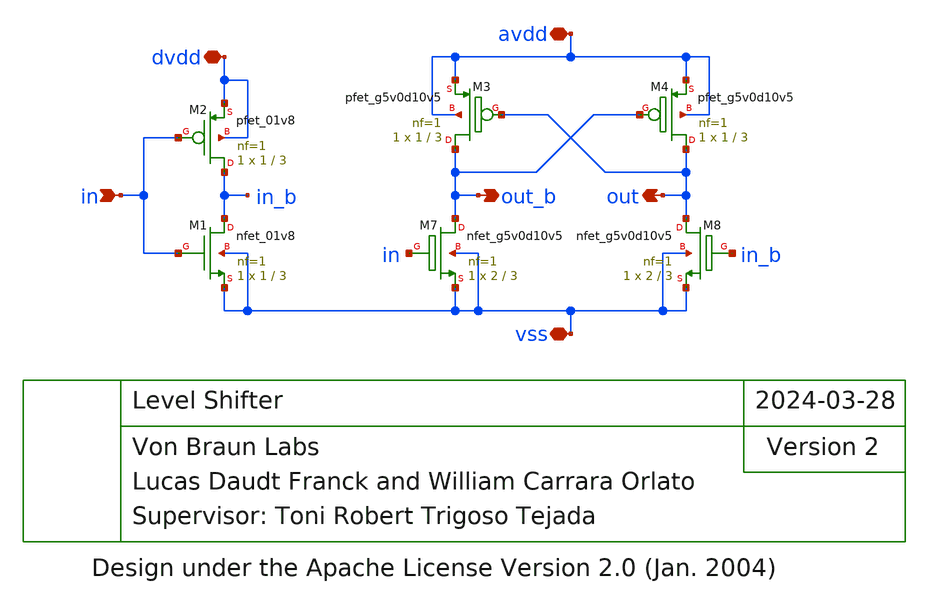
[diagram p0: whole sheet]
** sch_path: xschem/level_shifter.sch
* Design under the Apache License Version 2.0 (Jan. 2004)
**.subckt level_shifter avdd out_b out vss dvdd in
*.iopin avdd
*.opin out_b
*.opin out
*.iopin vss
*.iopin dvdd
*.ipin in
XM1 in_b in vss vss sky130_fd_pr__nfet_01v8 L=3 W=1 nf=1 ad='int((nf+1)/2) * W/nf * 0.29' as='int((nf+2)/2) * W/nf * 0.29'
+ pd='2*int((nf+1)/2) * (W/nf + 0.29)' ps='2*int((nf+2)/2) * (W/nf + 0.29)' nrd='0.29 / W' nrs='0.29 / W'
+ sa=0 sb=0 sd=0 mult=1 m=1
XM2 in_b in dvdd dvdd sky130_fd_pr__pfet_01v8 L=3 W=1 nf=1 ad='int((nf+1)/2) * W/nf * 0.29' as='int((nf+2)/2) * W/nf * 0.29'
+ pd='2*int((nf+1)/2) * (W/nf + 0.29)' ps='2*int((nf+2)/2) * (W/nf + 0.29)' nrd='0.29 / W' nrs='0.29 / W'
+ sa=0 sb=0 sd=0 mult=1 m=1
XM3 out_b out avdd avdd sky130_fd_pr__pfet_g5v0d10v5 L=3 W=1 nf=1 ad='int((nf+1)/2) * W/nf * 0.29' as='int((nf+2)/2) * W/nf * 0.29'
+ pd='2*int((nf+1)/2) * (W/nf + 0.29)' ps='2*int((nf+2)/2) * (W/nf + 0.29)' nrd='0.29 / W' nrs='0.29 / W'
+ sa=0 sb=0 sd=0 mult=1 m=1
XM4 out out_b avdd avdd sky130_fd_pr__pfet_g5v0d10v5 L=3 W=1 nf=1 ad='int((nf+1)/2) * W/nf * 0.29' as='int((nf+2)/2) * W/nf * 0.29'
+ pd='2*int((nf+1)/2) * (W/nf + 0.29)' ps='2*int((nf+2)/2) * (W/nf + 0.29)' nrd='0.29 / W' nrs='0.29 / W'
+ sa=0 sb=0 sd=0 mult=1 m=1
XM8 out in_b vss vss sky130_fd_pr__nfet_g5v0d10v5 L=3 W=2 nf=1 ad='int((nf+1)/2) * W/nf * 0.29' as='int((nf+2)/2) * W/nf * 0.29'
+ pd='2*int((nf+1)/2) * (W/nf + 0.29)' ps='2*int((nf+2)/2) * (W/nf + 0.29)' nrd='0.29 / W' nrs='0.29 / W'
+ sa=0 sb=0 sd=0 mult=1 m=1
XM7 out_b in vss vss sky130_fd_pr__nfet_g5v0d10v5 L=3 W=2 nf=1 ad='int((nf+1)/2) * W/nf * 0.29' as='int((nf+2)/2) * W/nf * 0.29'
+ pd='2*int((nf+1)/2) * (W/nf + 0.29)' ps='2*int((nf+2)/2) * (W/nf + 0.29)' nrd='0.29 / W' nrs='0.29 / W'
+ sa=0 sb=0 sd=0 mult=1 m=1
**.ends
.end
